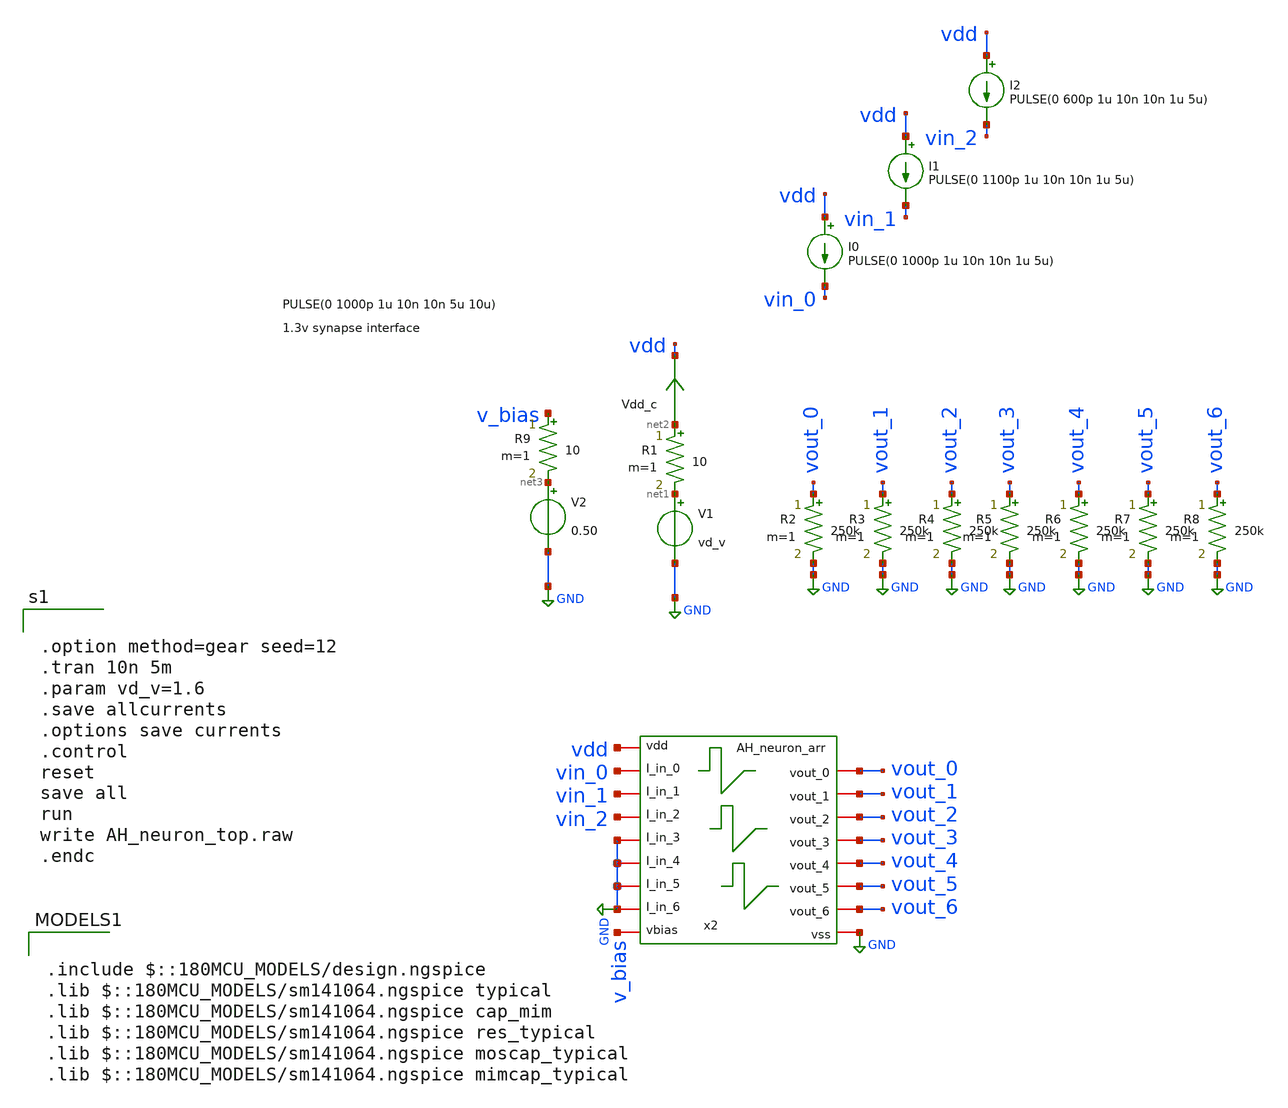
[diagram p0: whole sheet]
** sch_path: designs/libs/tb_core_analogs/tb_AH_neuron_arr/AH_neuron_arr.sch
**.subckt AH_neuron_arr
V1 net1 GND vd_v
Vdd_c net2 vdd 0
.save i(vdd_c)
I0 vdd vin_0 PULSE(0 1000p 1u 10n 10n 1u 5u)
R1 net2 net1 10 m=1
R2 vout_0 GND 250k m=1
x2 vdd GND vout_0 vin_0 vin_1 vout_1 vin_2 vout_2 vout_3 GND vout_4 GND GND vout_5 vout_6 GND v_bias
+ AH_neuron_arr
R3 vout_1 GND 250k m=1
R4 vout_2 GND 250k m=1
R5 vout_3 GND 250k m=1
R6 vout_4 GND 250k m=1
R7 vout_5 GND 250k m=1
R8 vout_6 GND 250k m=1
I1 vdd vin_1 PULSE(0 1100p 1u 10n 10n 1u 5u)
I2 vdd vin_2 PULSE(0 600p 1u 10n 10n 1u 5u)
V2 net3 GND 0.50
R9 v_bias net3 10 m=1
**** begin user architecture code


.option method=gear seed=12
.tran 10n 5m
.param vd_v=1.6
.save allcurrents
.options save currents
.control
reset
save all
run
write AH_neuron_top.raw
.endc



.include $::180MCU_MODELS/design.ngspice
.lib $::180MCU_MODELS/sm141064.ngspice typical
.lib $::180MCU_MODELS/sm141064.ngspice cap_mim
.lib $::180MCU_MODELS/sm141064.ngspice res_typical
.lib $::180MCU_MODELS/sm141064.ngspice moscap_typical
.lib $::180MCU_MODELS/sm141064.ngspice mimcap_typical

**** end user architecture code
**.ends

* expanding   symbol:  designs/libs/core_AH_neuron_arr/AH_neuron_arr.sym # of pins=17
** sym_path: designs/libs/core_AH_neuron_arr/AH_neuron_arr.sym
** sch_path: designs/libs/core_AH_neuron_arr/AH_neuron_arr.sch
.subckt AH_neuron_arr vdd vss vout_0 I_in_0 I_in_1 vout_1 I_in_2 vout_2 vout_3 I_in_3 vout_4 I_in_4
+ I_in_5 vout_5 vout_6 I_in_6 vbias
*.iopin vdd
*.iopin vss
*.iopin I_in_0
*.iopin vout_0
*.iopin I_in_6
*.iopin vout_6
*.iopin I_in_1
*.iopin vout_1
*.iopin I_in_2
*.iopin vout_2
*.iopin I_in_3
*.iopin vout_3
*.iopin I_in_4
*.iopin vout_4
*.iopin I_in_5
*.iopin vout_5
*.iopin vbias
x1 vdd I_in_3 vout_3 vss vbias AH_neuron
x2 vdd I_in_0 vout_0 vss vbias AH_neuron
x3 vdd I_in_1 vout_1 vss vbias AH_neuron
x4 vdd I_in_4 vout_4 vss vbias AH_neuron
x5 vdd I_in_2 vout_2 vss vbias AH_neuron
x6 vdd I_in_5 vout_5 vss vbias AH_neuron
x7 vdd I_in_6 vout_6 vss vbias AH_neuron
.ends

.GLOBAL GND
.end
